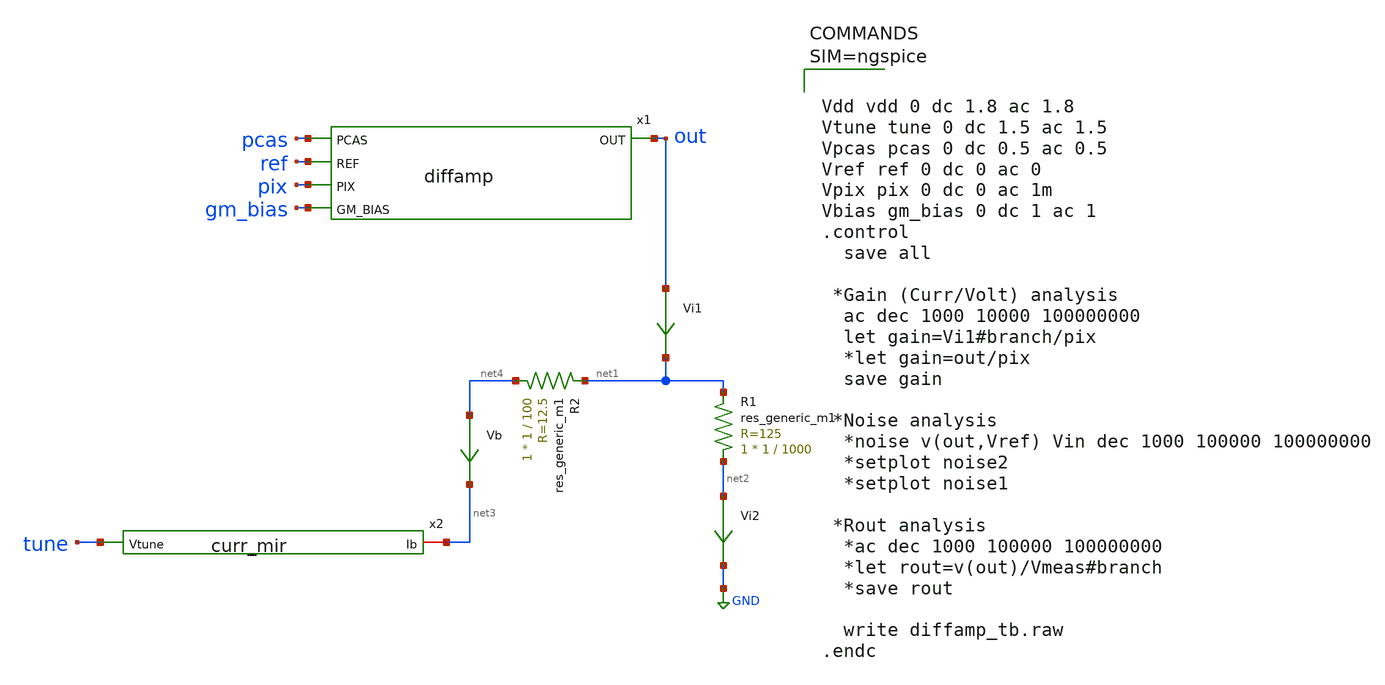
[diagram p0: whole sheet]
** sch_path: xschem/diffamp/diffamp_tb.sch
**.subckt diffamp_tb
Vb net4 net3 0
.save i(vb)
Vi2 net2 GND 0
.save i(vi2)
Vi1 out net1 0
.save i(vi1)
R1 net2 net1 sky130_fd_pr__res_generic_m1 W=1 L=1000 m=1
x1 pcas out ref pix gm_bias diffamp
x2 tune net3 curr_mir
R2 net4 net1 sky130_fd_pr__res_generic_m1 W=1 L=100 m=1
**** begin user architecture code



Vdd vdd 0 dc 1.8 ac 1.8
Vtune tune 0 dc 1.5 ac 1.5
Vpcas pcas 0 dc 0.5 ac 0.5
Vref ref 0 dc 0 ac 0
Vpix pix 0 dc 0 ac 1m
Vbias gm_bias 0 dc 1 ac 1
.control
  save all

 *Gain (Curr/Volt) analysis
  ac dec 1000 10000 100000000
  let gain=Vi1#branch/pix
  *let gain=out/pix
  save gain

 *Noise analysis
  *noise v(out,Vref) Vin dec 1000 100000 100000000
  *setplot noise2
  *setplot noise1

 *Rout analysis
  *ac dec 1000 100000 100000000
  *let rout=v(out)/Vmeas#branch
  *save rout

  write diffamp_tb.raw
.endc




** opencircuitdesign pdks install
.lib $::SKYWATER_MODELS/sky130.lib.spice tt


**** end user architecture code
**.ends

* expanding   symbol:  diffamp/diffamp.sym # of pins=5
** sym_path: xschem/diffamp/diffamp.sym
** sch_path: xschem/diffamp/diffamp.sch
.subckt diffamp PCAS OUT REF PIX GM_BIAS
*.ipin PCAS
*.ipin PIX
*.ipin REF
*.ipin GM_BIAS
*.opin OUT
XM4 OUT PCAS net2 net2 sky130_fd_pr__pfet_01v8_lvt L=3 W=90 nf=3 ad='int((3 + 1)/2) * 90 / 3 * 0.29'
+ as='int((3 + 2)/2) * 90 / 3 * 0.29' pd='2*int((3 + 1)/2) * (90 / 3 + 0.29)' ps='2*int((3 + 2)/2) * (90 / 3 + 0.29)'
+ nrd='0.29 / 90 ' nrs='0.29 / 90 ' sa=0 sb=0 sd=0 mult=1 m=1
XM5 net1 PCAS net3 net3 sky130_fd_pr__pfet_01v8_lvt L=3 W=90 nf=3 ad='int((3 + 1)/2) * 90 / 3 * 0.29'
+ as='int((3 + 2)/2) * 90 / 3 * 0.29' pd='2*int((3 + 1)/2) * (90 / 3 + 0.29)' ps='2*int((3 + 2)/2) * (90 / 3 + 0.29)'
+ nrd='0.29 / 90 ' nrs='0.29 / 90 ' sa=0 sb=0 sd=0 mult=1 m=1
XM6 OUT PIX net4 net4 sky130_fd_pr__nfet_01v8_lvt L=3.5 W=800 nf=35 ad='int((35 + 1)/2) * 800 / 35 * 0.29'
+ as='int((35 + 2)/2) * 800 / 35 * 0.29' pd='2*int((35 + 1)/2) * (800 / 35 + 0.29)' ps='2*int((35 + 2)/2) * (800 / 35 + 0.29)'
+ nrd='0.29 / 800 ' nrs='0.29 / 800 ' sa=0 sb=0 sd=0 mult=1 m=1
XM7 net1 REF net4 net4 sky130_fd_pr__nfet_01v8_lvt L=3.5 W=800 nf=35 ad='int((35 + 1)/2) * 800 / 35 * 0.29'
+ as='int((35 + 2)/2) * 800 / 35 * 0.29' pd='2*int((35 + 1)/2) * (800 / 35 + 0.29)' ps='2*int((35 + 2)/2) * (800 / 35 + 0.29)'
+ nrd='0.29 / 800 ' nrs='0.29 / 800 ' sa=0 sb=0 sd=0 mult=1 m=1
XM1 net3 net1 VDD VDD sky130_fd_pr__pfet_01v8_lvt L=15 W=90 nf=3 ad='int((3 + 1)/2) * 90 / 3 * 0.29'
+ as='int((3 + 2)/2) * 90 / 3 * 0.29' pd='2*int((3 + 1)/2) * (90 / 3 + 0.29)' ps='2*int((3 + 2)/2) * (90 / 3 + 0.29)'
+ nrd='0.29 / 90 ' nrs='0.29 / 90 ' sa=0 sb=0 sd=0 mult=1 m=1
XM2 net2 net1 VDD VDD sky130_fd_pr__pfet_01v8_lvt L=15 W=90 nf=3 ad='int((3 + 1)/2) * 90 / 3 * 0.29'
+ as='int((3 + 2)/2) * 90 / 3 * 0.29' pd='2*int((3 + 1)/2) * (90 / 3 + 0.29)' ps='2*int((3 + 2)/2) * (90 / 3 + 0.29)'
+ nrd='0.29 / 90 ' nrs='0.29 / 90 ' sa=0 sb=0 sd=0 mult=1 m=1
XM3 net4 GM_BIAS GND GND sky130_fd_pr__nfet_01v8_lvt L=15 W=20 nf=2 ad='int((2 + 1)/2) * 20 / 2 * 0.29'
+ as='int((2 + 2)/2) * 20 / 2 * 0.29' pd='2*int((2 + 1)/2) * (20 / 2 + 0.29)' ps='2*int((2 + 2)/2) * (20 / 2 + 0.29)'
+ nrd='0.29 / 20 ' nrs='0.29 / 20 ' sa=0 sb=0 sd=0 mult=1 m=1
.ends


* expanding   symbol:  current_mirror/curr_mir.sym # of pins=2
** sym_path: xschem/current_mirror/curr_mir.sym
** sch_path: xschem/current_mirror/curr_mir.sch
.subckt curr_mir Vtune Ib
*.ipin Vtune
*.iopin Ib
XM1 net1 net1 GND GND sky130_fd_pr__nfet_01v8_lvt L=2 W=50 nf=1 ad='int((1 + 1)/2) * 50 / 1 * 0.29' as='int((1 + 2)/2) * 50 / 1 * 0.29'
+ pd='2*int((1 + 1)/2) * (50 / 1 + 0.29)' ps='2*int((1 + 2)/2) * (50 / 1 + 0.29)' nrd='0.29 / 50 ' nrs='0.29 / 50 '
+ sa=0 sb=0 sd=0 mult=1 m=1
XM2 Ib net1 GND GND sky130_fd_pr__nfet_01v8_lvt L=25 W=4 nf=1 ad='int((1 + 1)/2) * 4 / 1 * 0.29' as='int((1 + 2)/2) * 4 / 1 * 0.29'
+ pd='2*int((1 + 1)/2) * (4 / 1 + 0.29)' ps='2*int((1 + 2)/2) * (4 / 1 + 0.29)' nrd='0.29 / 4 ' nrs='0.29 / 4 '
+ sa=0 sb=0 sd=0 mult=1 m=1
XM10 net1 Vtune VDD VDD sky130_fd_pr__pfet_01v8_lvt L=10 W=10 nf=1 ad='int((1 + 1)/2) * 10 / 1 * 0.29'
+ as='int((1 + 2)/2) * 10 / 1 * 0.29' pd='2*int((1 + 1)/2) * (10 / 1 + 0.29)' ps='2*int((1 + 2)/2) * (10 / 1 + 0.29)'
+ nrd='0.29 / 10 ' nrs='0.29 / 10 ' sa=0 sb=0 sd=0 mult=1 m=1
.ends

.GLOBAL GND
.GLOBAL VDD
.end
